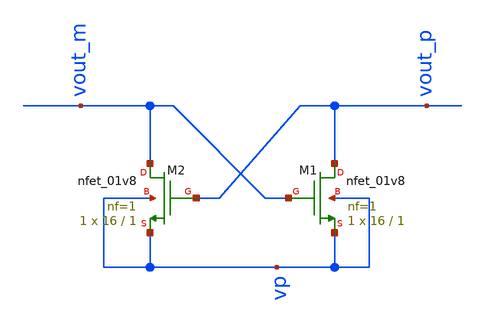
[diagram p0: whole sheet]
** sch_path: crosscoupled.sch
**.subckt crosscoupled
XM1 vout_p vout_m vp vp sky130_fd_pr__nfet_01v8 L=1 W=16 nf=1 ad='int((nf+1)/2) * W/nf * 0.29' as='int((nf+2)/2) * W/nf * 0.29'
+ pd='2*int((nf+1)/2) * (W/nf + 0.29)' ps='2*int((nf+2)/2) * (W/nf + 0.29)' nrd='0.29 / W' nrs='0.29 / W'
+ sa=0 sb=0 sd=0 mult=1 m=1
XM2 vout_m vout_p vp vp sky130_fd_pr__nfet_01v8 L=1 W=16 nf=1 ad='int((nf+1)/2) * W/nf * 0.29' as='int((nf+2)/2) * W/nf * 0.29'
+ pd='2*int((nf+1)/2) * (W/nf + 0.29)' ps='2*int((nf+2)/2) * (W/nf + 0.29)' nrd='0.29 / W' nrs='0.29 / W'
+ sa=0 sb=0 sd=0 mult=1 m=1
**.ends
.end
